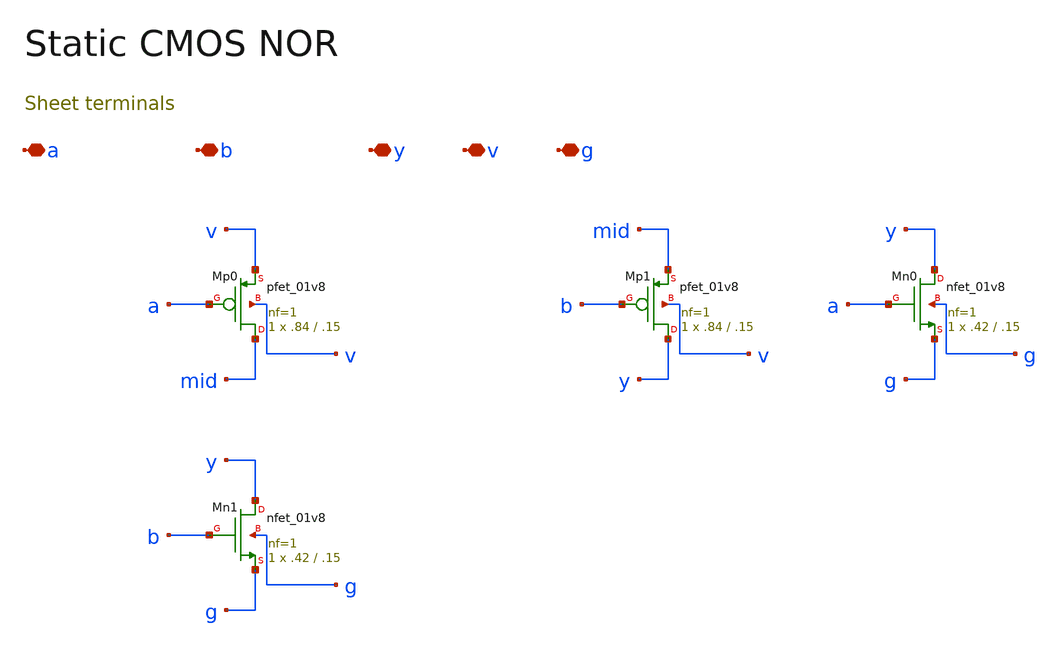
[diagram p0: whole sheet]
** sch_path: review/xschem/nor2.sch
**.subckt nor2 a b y v g
*.iopin a
*.iopin b
*.iopin y
*.iopin v
*.iopin g
XMp0 mid a v v sky130_fd_pr__pfet_01v8 L=.15 W=.84 nf=1 ad='int((nf+1)/2) * W/nf * 0.29' as='int((nf+2)/2) * W/nf * 0.29'
+ pd='2*int((nf+1)/2) * (W/nf + 0.29)' ps='2*int((nf+2)/2) * (W/nf + 0.29)' nrd='0.29 / W' nrs='0.29 / W'
+ sa=0 sb=0 sd=0 mult=1 m=1
XMp1 y b mid v sky130_fd_pr__pfet_01v8 L=.15 W=.84 nf=1 ad='int((nf+1)/2) * W/nf * 0.29' as='int((nf+2)/2) * W/nf * 0.29'
+ pd='2*int((nf+1)/2) * (W/nf + 0.29)' ps='2*int((nf+2)/2) * (W/nf + 0.29)' nrd='0.29 / W' nrs='0.29 / W'
+ sa=0 sb=0 sd=0 mult=1 m=1
XMn0 y a g g sky130_fd_pr__nfet_01v8 L=.15 W=.42 nf=1 ad='int((1 + 1)/2) * .42 / 1 * 0.29' as='int((1 + 2)/2) * .42 / 1 * 0.29'
+ pd='2*int((1 + 1)/2) * (.42 / 1 + 0.29)' ps='2*int((1 + 2)/2) * (.42 / 1 + 0.29)' nrd='0.29 / .42 ' nrs='0.29 / .42 '
+ sa=0 sb=0 sd=0 mult=1 m=1
XMn1 y b g g sky130_fd_pr__nfet_01v8 L=.15 W=.42 nf=1 ad='int((1 + 1)/2) * .42 / 1 * 0.29' as='int((1 + 2)/2) * .42 / 1 * 0.29'
+ pd='2*int((1 + 1)/2) * (.42 / 1 + 0.29)' ps='2*int((1 + 2)/2) * (.42 / 1 + 0.29)' nrd='0.29 / .42 ' nrs='0.29 / .42 '
+ sa=0 sb=0 sd=0 mult=1 m=1
**.ends
.end
